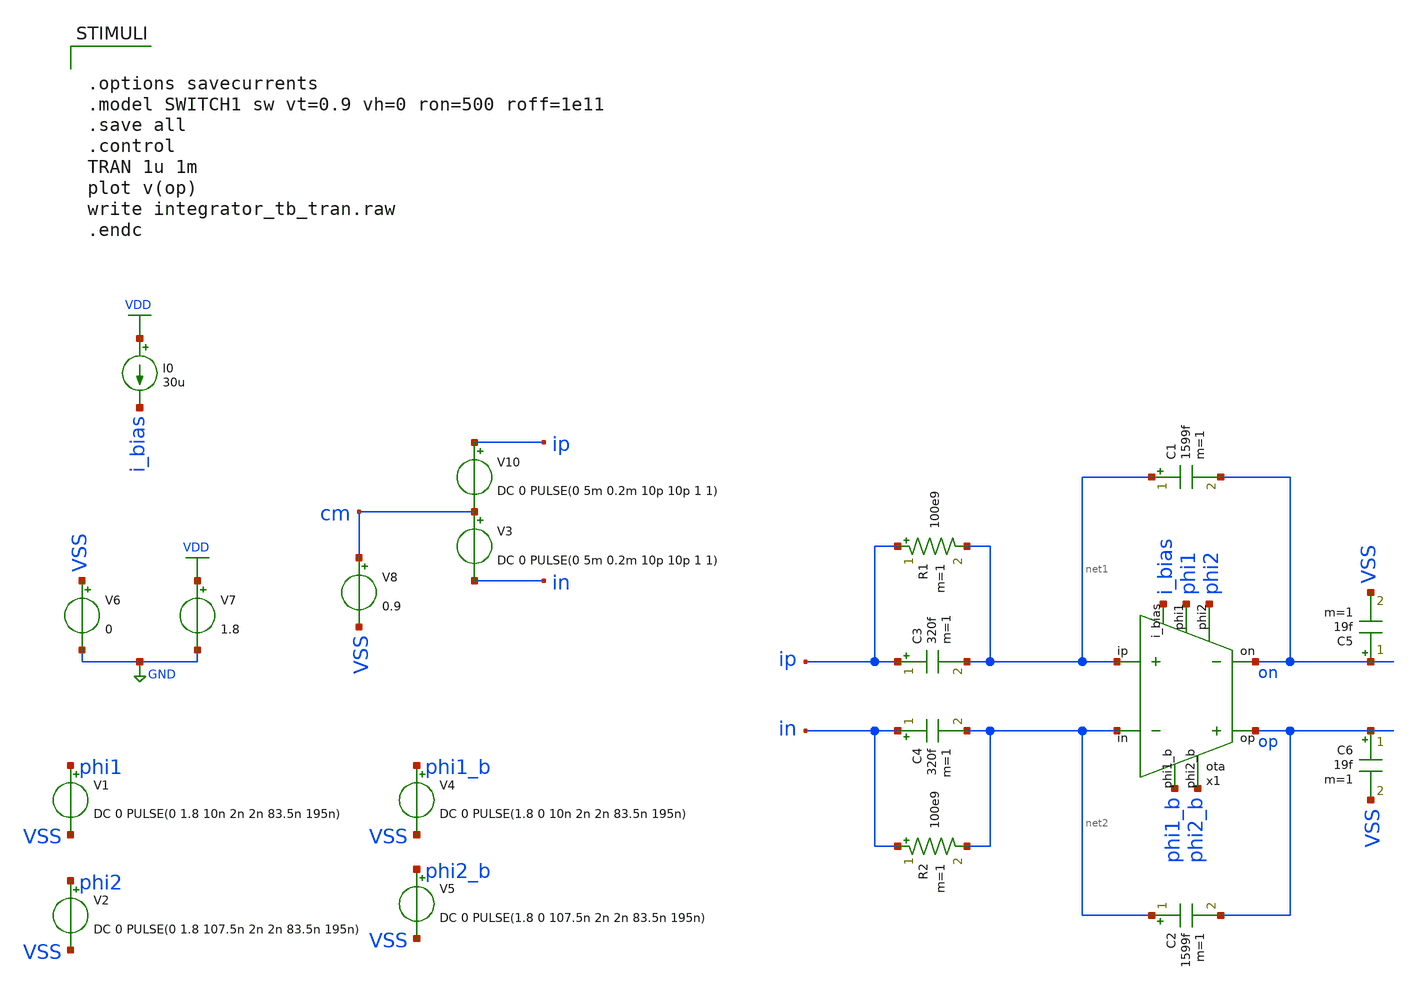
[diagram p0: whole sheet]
** sch_path: verification/schematic/integrator_tb.sch
**.subckt integrator_tb
V6 VSS GND 0
V7 VDD GND 1.8
V8 cm VSS 0.9
V10 ip cm DC 0 PULSE(0 5m 0.2m 10p 10p 1 1)
V1 phi1 VSS DC 0 PULSE(0 1.8 10n 2n 2n 83.5n 195n)
V2 phi2 VSS DC 0 PULSE(0 1.8 107.5n 2n 2n 83.5n 195n)
V3 cm in DC 0 PULSE(0 5m 0.2m 10p 10p 1 1)
V4 phi1_b VSS DC 0 PULSE(1.8 0 10n 2n 2n 83.5n 195n)
V5 phi2_b VSS DC 0 PULSE(1.8 0 107.5n 2n 2n 83.5n 195n)
x1 i_bias net1 net2 phi1 phi1_b phi2 phi2_b op on 50 350 VDD VSS ota
I0 VDD i_bias 30u
C3 ip net1 320f m=1
C4 in net2 320f m=1
R1 ip net1 100e9 m=1
R2 in net2 100e9 m=1
C1 net1 on 1599f m=1
C2 net2 op 1599f m=1
C5 on VSS 19f m=1
C6 op VSS 19f m=1
**** begin user architecture code

** opencircuitdesign pdks install
.lib /farmshare/home/classes/ee/372/PDKs/open_pdks_1.0.310/sky130/sky130A/libs.tech/ngspice/sky130.lib.spice tt



.options savecurrents
.model SWITCH1 sw vt=0.9 vh=0 ron=500 roff=1e11
.save all
.control
TRAN 1u 1m
plot v(op)
write integrator_tb_tran.raw
.endc


**** end user architecture code
**.ends

* expanding   symbol:  ota.sym # of pins=9
** sym_path: design/schematic/ota.sym
** sch_path: design/schematic/ota.sch
.subckt ota i_bias ip in phi1 phi1_b phi2 phi2_b op on C_CMFB C_COMP VDD VSS  C_CMFB=50 C_COMP=350
*.ipin ip
*.ipin in
*.ipin phi1
*.ipin phi1_b
*.ipin phi2
*.ipin phi2_b
*.opin op
*.opin on
*.ipin i_bias
x3 phi1 phi1_b op on bias_e bias_a cmc phi2 phi2_b 10 VDD VSS sc_cmfb
x1 bias_a bias_b bias_c bias_d bias_e i_bias VDD VSS folded_cascode_3_bias
x2 cmc ip in bias_a bias_b bias_c bias_d op on VDD VSS folded_cascode_3_core
.ends


* expanding   symbol:  sc_cmfb.sym # of pins=9
** sym_path: design/schematic/sc_cmfb.sym
** sch_path: design/schematic/sc_cmfb.sch
.subckt sc_cmfb phi1 phi1_b op on cm bias_a cmc phi2 phi2_b MF VDD VSS  MF=50
*.ipin on
*.ipin cm
*.ipin bias_a
*.ipin op
*.opin cmc
*.ipin phi2_b
*.ipin phi2
*.ipin phi1_b
*.ipin phi1
x1 net1 cm phi1 phi1_b VDD GND 1 5.3 0.15 13.7 0.15 transmission_gate
x2 net2 bias_a phi1 phi1_b VDD GND 1 5.3 0.15 13.7 0.15 transmission_gate
x3 net3 cm phi1 phi1_b VDD GND 1 5.3 0.15 13.7 0.15 transmission_gate
x4 op net1 phi2 phi2_b VDD GND 1 5.3 0.15 13.7 0.15 transmission_gate
x5 cmc net2 phi2 phi2_b VDD GND 1 5.3 0.15 13.7 0.15 transmission_gate
x6 on net3 phi2 phi2_b VDD GND 1 5.3 0.15 13.7 0.15 transmission_gate
XC1 net1 net2 sky130_fd_pr__cap_mim_m3_1 W=1 L=1 MF='MF' m='MF'
XC2 net2 net3 sky130_fd_pr__cap_mim_m3_1 W=1 L=1 MF='MF' m='MF'
XC3 op cmc sky130_fd_pr__cap_mim_m3_1 W=1 L=1 MF='2*MF' m='2*MF'
XC4 cmc on sky130_fd_pr__cap_mim_m3_1 W=1 L=1 MF='2*MF' m='2*MF'
.ends


* expanding   symbol:  folded_cascode_3_bias.sym # of pins=6
** sym_path: design/schematic/folded_cascode_3_bias.sym
** sch_path: design/schematic/folded_cascode_3_bias.sch
.subckt folded_cascode_3_bias bias_a bias_b bias_c bias_d bias_e i_bias VDD VSS
*.opin bias_a
*.opin bias_b
*.opin bias_c
*.opin bias_d
*.opin bias_e
*.ipin i_bias
XM22 bias_b bias_c net3 VDD sky130_fd_pr__pfet_01v8 L=0.8 W=2 nf=1 ad='int((nf+1)/2) * W/nf * 0.29' as='int((nf+2)/2) * W/nf * 0.29'
+ pd='2*int((nf+1)/2) * (W/nf + 0.29)' ps='2*int((nf+2)/2) * (W/nf + 0.29)' nrd='0.29 / W' nrs='0.29 / W'
+ sa=0 sb=0 sd=0 mult=6 m=6
XM26 net5 bias_c net1 VDD sky130_fd_pr__pfet_01v8 L=0.8 W=2 nf=1 ad='int((nf+1)/2) * W/nf * 0.29' as='int((nf+2)/2) * W/nf * 0.29'
+ pd='2*int((nf+1)/2) * (W/nf + 0.29)' ps='2*int((nf+2)/2) * (W/nf + 0.29)' nrd='0.29 / W' nrs='0.29 / W'
+ sa=0 sb=0 sd=0 mult=6 m=6
XM32 bias_e bias_c net2 VDD sky130_fd_pr__pfet_01v8 L=0.8 W=2 nf=1 ad='int((nf+1)/2) * W/nf * 0.29' as='int((nf+2)/2) * W/nf * 0.29'
+ pd='2*int((nf+1)/2) * (W/nf + 0.29)' ps='2*int((nf+2)/2) * (W/nf + 0.29)' nrd='0.29 / W' nrs='0.29 / W'
+ sa=0 sb=0 sd=0 mult=6 m=6
XM33 bias_e bias_e VSS VSS sky130_fd_pr__nfet_01v8 L=0.8 W=2 nf=1 ad='int((nf+1)/2) * W/nf * 0.29' as='int((nf+2)/2) * W/nf * 0.29'
+ pd='2*int((nf+1)/2) * (W/nf + 0.29)' ps='2*int((nf+2)/2) * (W/nf + 0.29)' nrd='0.29 / W' nrs='0.29 / W'
+ sa=0 sb=0 sd=0 mult=2 m=2
XM21 net3 bias_b VDD VDD sky130_fd_pr__pfet_01v8_lvt L=0.8 W=2 nf=1 ad='int((nf+1)/2) * W/nf * 0.29'
+ as='int((nf+2)/2) * W/nf * 0.29' pd='2*int((nf+1)/2) * (W/nf + 0.29)' ps='2*int((nf+2)/2) * (W/nf + 0.29)'
+ nrd='0.29 / W' nrs='0.29 / W' sa=0 sb=0 sd=0 mult=6 m=6
XM25 net1 bias_b VDD VDD sky130_fd_pr__pfet_01v8_lvt L=0.8 W=2 nf=1 ad='int((nf+1)/2) * W/nf * 0.29'
+ as='int((nf+2)/2) * W/nf * 0.29' pd='2*int((nf+1)/2) * (W/nf + 0.29)' ps='2*int((nf+2)/2) * (W/nf + 0.29)'
+ nrd='0.29 / W' nrs='0.29 / W' sa=0 sb=0 sd=0 mult=6 m=6
XM31 net2 bias_b VDD VDD sky130_fd_pr__pfet_01v8_lvt L=0.8 W=2 nf=1 ad='int((nf+1)/2) * W/nf * 0.29'
+ as='int((nf+2)/2) * W/nf * 0.29' pd='2*int((nf+1)/2) * (W/nf + 0.29)' ps='2*int((nf+2)/2) * (W/nf + 0.29)'
+ nrd='0.29 / W' nrs='0.29 / W' sa=0 sb=0 sd=0 mult=6 m=6
XM1 bias_b bias_b bias_c VSS sky130_fd_pr__nfet_01v8_lvt L=0.8 W=2 nf=1 ad='int((nf+1)/2) * W/nf * 0.29'
+ as='int((nf+2)/2) * W/nf * 0.29' pd='2*int((nf+1)/2) * (W/nf + 0.29)' ps='2*int((nf+2)/2) * (W/nf + 0.29)'
+ nrd='0.29 / W' nrs='0.29 / W' sa=0 sb=0 sd=0 mult=56 m=56
XM2 net5 net5 bias_d VSS sky130_fd_pr__nfet_01v8 L=0.8 W=2 nf=1 ad='int((nf+1)/2) * W/nf * 0.29' as='int((nf+2)/2) * W/nf * 0.29'
+ pd='2*int((nf+1)/2) * (W/nf + 0.29)' ps='2*int((nf+2)/2) * (W/nf + 0.29)' nrd='0.29 / W' nrs='0.29 / W'
+ sa=0 sb=0 sd=0 mult=50 m=50
XM3 bias_d net5 bias_a VSS sky130_fd_pr__nfet_01v8 L=0.8 W=2 nf=1 ad='int((nf+1)/2) * W/nf * 0.29' as='int((nf+2)/2) * W/nf * 0.29'
+ pd='2*int((nf+1)/2) * (W/nf + 0.29)' ps='2*int((nf+2)/2) * (W/nf + 0.29)' nrd='0.29 / W' nrs='0.29 / W'
+ sa=0 sb=0 sd=0 mult=2 m=2
XM4 bias_a bias_d net4 VSS sky130_fd_pr__nfet_01v8 L=0.8 W=2 nf=1 ad='int((nf+1)/2) * W/nf * 0.29' as='int((nf+2)/2) * W/nf * 0.29'
+ pd='2*int((nf+1)/2) * (W/nf + 0.29)' ps='2*int((nf+2)/2) * (W/nf + 0.29)' nrd='0.29 / W' nrs='0.29 / W'
+ sa=0 sb=0 sd=0 mult=18 m=18
XM5 net4 bias_a VSS VSS sky130_fd_pr__nfet_01v8 L=0.8 W=2 nf=1 ad='int((nf+1)/2) * W/nf * 0.29' as='int((nf+2)/2) * W/nf * 0.29'
+ pd='2*int((nf+1)/2) * (W/nf + 0.29)' ps='2*int((nf+2)/2) * (W/nf + 0.29)' nrd='0.29 / W' nrs='0.29 / W'
+ sa=0 sb=0 sd=0 mult=18 m=18
XM6 bias_c i_bias VSS VSS sky130_fd_pr__nfet_01v8 L=0.8 W=2 nf=1 ad='int((nf+1)/2) * W/nf * 0.29' as='int((nf+2)/2) * W/nf * 0.29'
+ pd='2*int((nf+1)/2) * (W/nf + 0.29)' ps='2*int((nf+2)/2) * (W/nf + 0.29)' nrd='0.29 / W' nrs='0.29 / W'
+ sa=0 sb=0 sd=0 mult=18 m=18
XM7 i_bias i_bias VSS VSS sky130_fd_pr__nfet_01v8 L=0.8 W=2 nf=1 ad='int((nf+1)/2) * W/nf * 0.29' as='int((nf+2)/2) * W/nf * 0.29'
+ pd='2*int((nf+1)/2) * (W/nf + 0.29)' ps='2*int((nf+2)/2) * (W/nf + 0.29)' nrd='0.29 / W' nrs='0.29 / W'
+ sa=0 sb=0 sd=0 mult=18 m=18
.ends


* expanding   symbol:  folded_cascode_3_core.sym # of pins=9
** sym_path: design/schematic/folded_cascode_3_core.sym
** sch_path: design/schematic/folded_cascode_3_core.sch
.subckt folded_cascode_3_core cmc ip in bias_a bias_b bias_c bias_d op on VDD VSS
*.ipin cmc
*.ipin ip
*.ipin in
*.ipin bias_a
*.ipin bias_b
*.ipin bias_c
*.ipin bias_d
*.opin op
*.opin on
XM1 net2 ip net1 VSS sky130_fd_pr__nfet_01v8_lvt L=0.2 W=1.2 nf=1 ad='int((nf+1)/2) * W/nf * 0.29' as='int((nf+2)/2) * W/nf * 0.29'
+ pd='2*int((nf+1)/2) * (W/nf + 0.29)' ps='2*int((nf+2)/2) * (W/nf + 0.29)' nrd='0.29 / W' nrs='0.29 / W'
+ sa=0 sb=0 sd=0 mult=6 m=6
XM2 net3 in net1 VSS sky130_fd_pr__nfet_01v8_lvt L=0.2 W=1.2 nf=1 ad='int((nf+1)/2) * W/nf * 0.29' as='int((nf+2)/2) * W/nf * 0.29'
+ pd='2*int((nf+1)/2) * (W/nf + 0.29)' ps='2*int((nf+2)/2) * (W/nf + 0.29)' nrd='0.29 / W' nrs='0.29 / W'
+ sa=0 sb=0 sd=0 mult=6 m=6
XM6 net1 cmc VSS VSS sky130_fd_pr__nfet_01v8 L=0.6 W=1.4 nf=1 ad='int((nf+1)/2) * W/nf * 0.29' as='int((nf+2)/2) * W/nf * 0.29'
+ pd='2*int((nf+1)/2) * (W/nf + 0.29)' ps='2*int((nf+2)/2) * (W/nf + 0.29)' nrd='0.29 / W' nrs='0.29 / W'
+ sa=0 sb=0 sd=0 mult=48 m=48
XM5 net1 bias_a VSS VSS sky130_fd_pr__nfet_01v8 L=0.6 W=1.4 nf=1 ad='int((nf+1)/2) * W/nf * 0.29' as='int((nf+2)/2) * W/nf * 0.29'
+ pd='2*int((nf+1)/2) * (W/nf + 0.29)' ps='2*int((nf+2)/2) * (W/nf + 0.29)' nrd='0.29 / W' nrs='0.29 / W'
+ sa=0 sb=0 sd=0 mult=48 m=48
XM11 net2 bias_b VDD VDD sky130_fd_pr__pfet_01v8_lvt L=0.6 W=1.4 nf=1 ad='int((nf+1)/2) * W/nf * 0.29'
+ as='int((nf+2)/2) * W/nf * 0.29' pd='2*int((nf+1)/2) * (W/nf + 0.29)' ps='2*int((nf+2)/2) * (W/nf + 0.29)'
+ nrd='0.29 / W' nrs='0.29 / W' sa=0 sb=0 sd=0 mult=24 m=24
XM12 net3 bias_b VDD VDD sky130_fd_pr__pfet_01v8_lvt L=0.6 W=1.4 nf=1 ad='int((nf+1)/2) * W/nf * 0.29'
+ as='int((nf+2)/2) * W/nf * 0.29' pd='2*int((nf+1)/2) * (W/nf + 0.29)' ps='2*int((nf+2)/2) * (W/nf + 0.29)'
+ nrd='0.29 / W' nrs='0.29 / W' sa=0 sb=0 sd=0 mult=24 m=24
XM1A on bias_c net2 VDD sky130_fd_pr__pfet_01v8 L=0.6 W=1.4 nf=1 ad='int((nf+1)/2) * W/nf * 0.29' as='int((nf+2)/2) * W/nf * 0.29'
+ pd='2*int((nf+1)/2) * (W/nf + 0.29)' ps='2*int((nf+2)/2) * (W/nf + 0.29)' nrd='0.29 / W' nrs='0.29 / W'
+ sa=0 sb=0 sd=0 mult=20 m=20
XM8 op bias_c net3 VDD sky130_fd_pr__pfet_01v8 L=0.6 W=1.4 nf=1 ad='int((nf+1)/2) * W/nf * 0.29' as='int((nf+2)/2) * W/nf * 0.29'
+ pd='2*int((nf+1)/2) * (W/nf + 0.29)' ps='2*int((nf+2)/2) * (W/nf + 0.29)' nrd='0.29 / W' nrs='0.29 / W'
+ sa=0 sb=0 sd=0 mult=20 m=20
XM3A on bias_d net4 VSS sky130_fd_pr__nfet_01v8 L=0.6 W=1.4 nf=1 ad='int((nf+1)/2) * W/nf * 0.29' as='int((nf+2)/2) * W/nf * 0.29'
+ pd='2*int((nf+1)/2) * (W/nf + 0.29)' ps='2*int((nf+2)/2) * (W/nf + 0.29)' nrd='0.29 / W' nrs='0.29 / W'
+ sa=0 sb=0 sd=0 mult=36 m=36
XM7 op bias_d net5 VSS sky130_fd_pr__nfet_01v8 L=0.6 W=1.4 nf=1 ad='int((nf+1)/2) * W/nf * 0.29' as='int((nf+2)/2) * W/nf * 0.29'
+ pd='2*int((nf+1)/2) * (W/nf + 0.29)' ps='2*int((nf+2)/2) * (W/nf + 0.29)' nrd='0.29 / W' nrs='0.29 / W'
+ sa=0 sb=0 sd=0 mult=36 m=36
XM3 net4 bias_a VSS VSS sky130_fd_pr__nfet_01v8 L=0.6 W=1.4 nf=1 ad='int((nf+1)/2) * W/nf * 0.29' as='int((nf+2)/2) * W/nf * 0.29'
+ pd='2*int((nf+1)/2) * (W/nf + 0.29)' ps='2*int((nf+2)/2) * (W/nf + 0.29)' nrd='0.29 / W' nrs='0.29 / W'
+ sa=0 sb=0 sd=0 mult=36 m=36
XM4 net5 bias_a VSS VSS sky130_fd_pr__nfet_01v8 L=0.6 W=1.4 nf=1 ad='int((nf+1)/2) * W/nf * 0.29' as='int((nf+2)/2) * W/nf * 0.29'
+ pd='2*int((nf+1)/2) * (W/nf + 0.29)' ps='2*int((nf+2)/2) * (W/nf + 0.29)' nrd='0.29 / W' nrs='0.29 / W'
+ sa=0 sb=0 sd=0 mult=36 m=36
.ends


* expanding   symbol:  transmission_gate.sym # of pins=4
** sym_path: design/schematic/transmission_gate.sym
** sch_path: design/schematic/transmission_gate.sch
.subckt transmission_gate in out en en_b VDD VSS N W_N L_N W_P L_P    N=1 W_N=5.3 L_N=0.15 W_P=13.7
+ L_P=0.15
*.iopin in
*.iopin out
*.ipin en
*.ipin en_b
XM1 out en in VSS sky130_fd_pr__nfet_01v8 L=L_N W=W_N nf=1 ad='int((nf+1)/2) * W/nf * 0.29' as='int((nf+2)/2) * W/nf * 0.29'
+ pd='2*int((nf+1)/2) * (W/nf + 0.29)' ps='2*int((nf+2)/2) * (W/nf + 0.29)' nrd='0.29 / W' nrs='0.29 / W'
+ sa=0 sb=0 sd=0 mult=N m=N
XM2 out en_b in VDD sky130_fd_pr__pfet_01v8 L=L_P W=W_P nf=1 ad='int((nf+1)/2) * W/nf * 0.29' as='int((nf+2)/2) * W/nf * 0.29'
+ pd='2*int((nf+1)/2) * (W/nf + 0.29)' ps='2*int((nf+2)/2) * (W/nf + 0.29)' nrd='0.29 / W' nrs='0.29 / W'
+ sa=0 sb=0 sd=0 mult=N m=N
.ends

.GLOBAL VDD
.GLOBAL GND
.end
